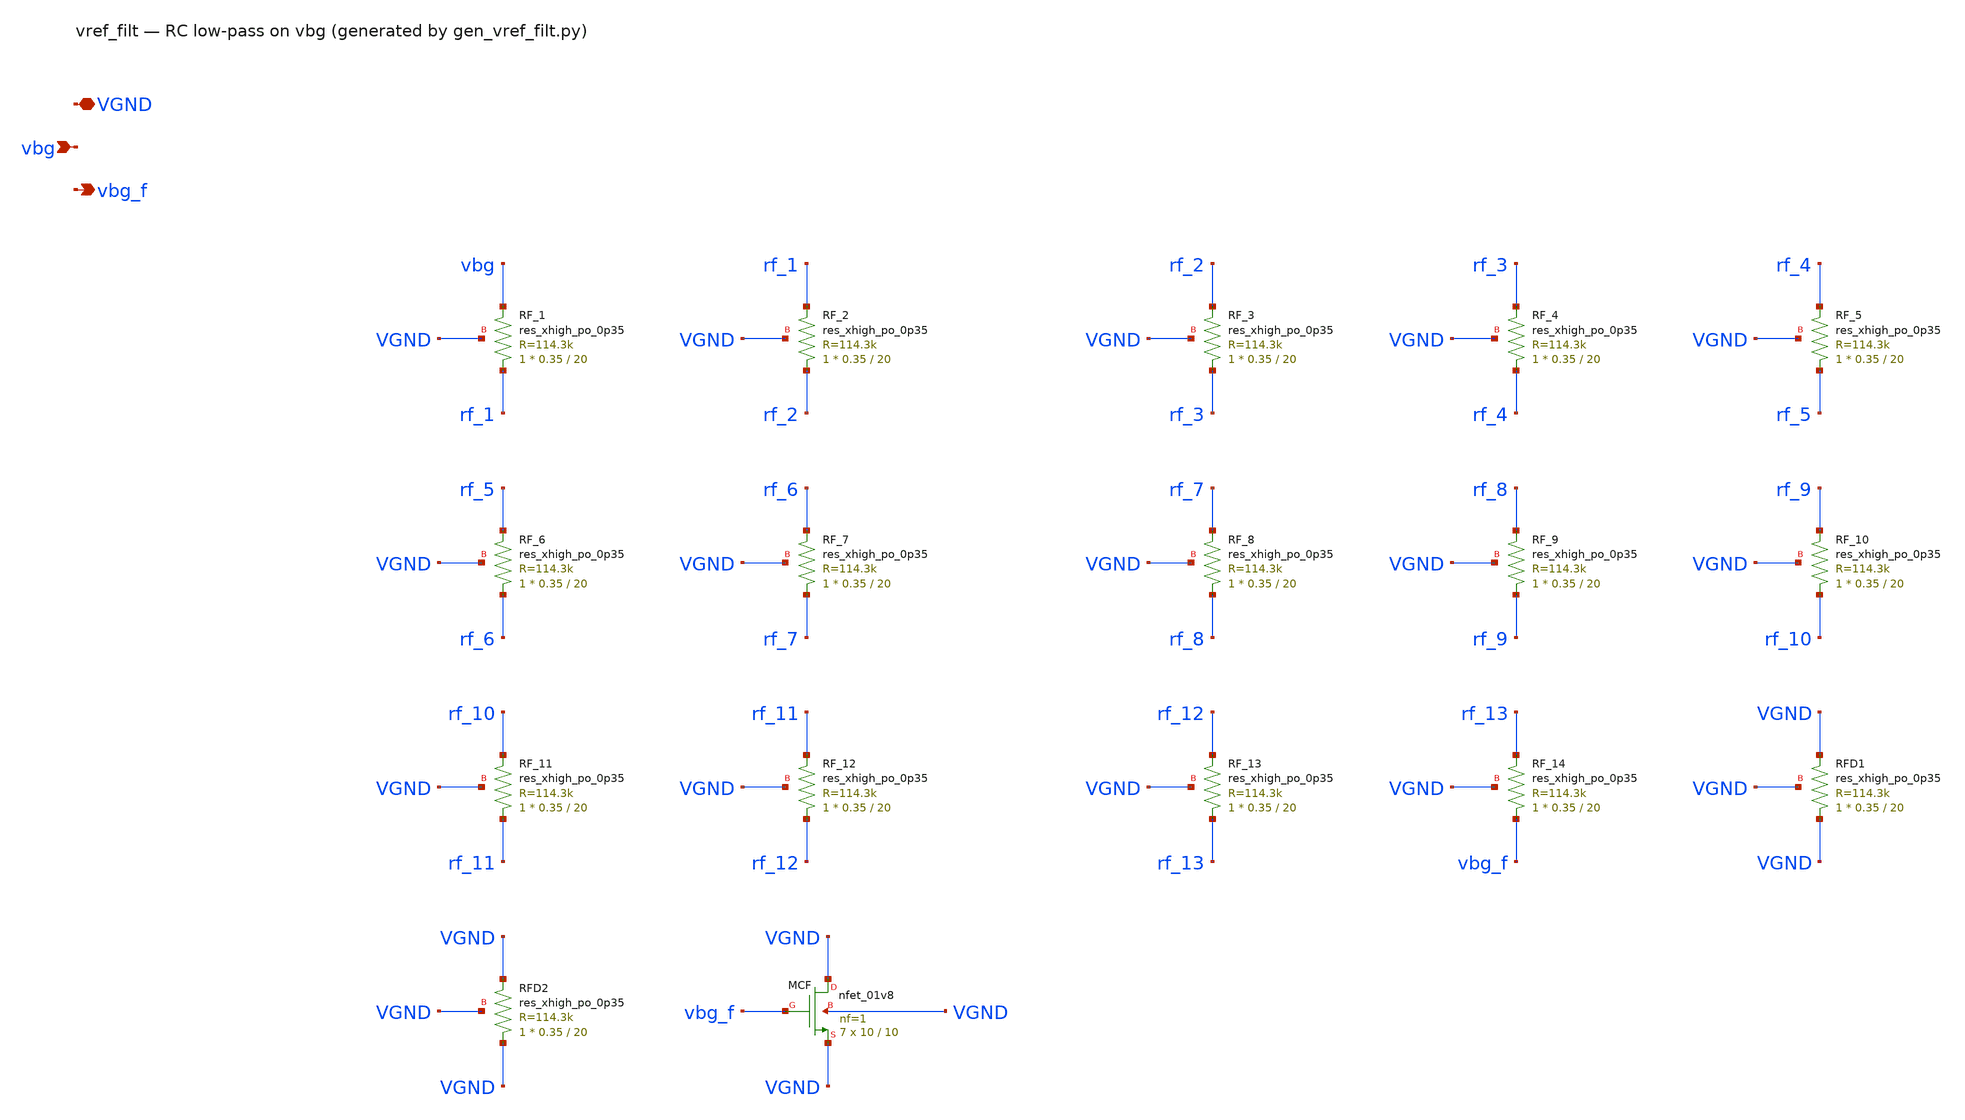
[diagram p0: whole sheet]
** sch_path: xschem/vref_filt.sch
**.subckt vref_filt VGND vbg vbg_f
*.iopin VGND
*.ipin vbg
*.opin vbg_f
XRF_1 rf_1 vbg VGND sky130_fd_pr__res_xhigh_po_0p35 L=20 mult=1 m=1
XRF_2 rf_2 rf_1 VGND sky130_fd_pr__res_xhigh_po_0p35 L=20 mult=1 m=1
XRF_3 rf_3 rf_2 VGND sky130_fd_pr__res_xhigh_po_0p35 L=20 mult=1 m=1
XRF_4 rf_4 rf_3 VGND sky130_fd_pr__res_xhigh_po_0p35 L=20 mult=1 m=1
XRF_5 rf_5 rf_4 VGND sky130_fd_pr__res_xhigh_po_0p35 L=20 mult=1 m=1
XRF_6 rf_6 rf_5 VGND sky130_fd_pr__res_xhigh_po_0p35 L=20 mult=1 m=1
XRF_7 rf_7 rf_6 VGND sky130_fd_pr__res_xhigh_po_0p35 L=20 mult=1 m=1
XRF_8 rf_8 rf_7 VGND sky130_fd_pr__res_xhigh_po_0p35 L=20 mult=1 m=1
XRF_9 rf_9 rf_8 VGND sky130_fd_pr__res_xhigh_po_0p35 L=20 mult=1 m=1
XRF_10 rf_10 rf_9 VGND sky130_fd_pr__res_xhigh_po_0p35 L=20 mult=1 m=1
XRF_11 rf_11 rf_10 VGND sky130_fd_pr__res_xhigh_po_0p35 L=20 mult=1 m=1
XRF_12 rf_12 rf_11 VGND sky130_fd_pr__res_xhigh_po_0p35 L=20 mult=1 m=1
XRF_13 rf_13 rf_12 VGND sky130_fd_pr__res_xhigh_po_0p35 L=20 mult=1 m=1
XRF_14 vbg_f rf_13 VGND sky130_fd_pr__res_xhigh_po_0p35 L=20 mult=1 m=1
XRFD1 VGND VGND VGND sky130_fd_pr__res_xhigh_po_0p35 L=20 mult=1 m=1
XRFD2 VGND VGND VGND sky130_fd_pr__res_xhigh_po_0p35 L=20 mult=1 m=1
XMCF VGND vbg_f VGND VGND sky130_fd_pr__nfet_01v8 L=10 W=10 nf=1 ad='int((1 + 1)/2) * 10 / 1 * 0.29'
+ as='int((1 + 2)/2) * 10 / 1 * 0.29' pd='2*int((1 + 1)/2) * (10 / 1 + 0.29)' ps='2*int((1 + 2)/2) * (10 / 1 + 0.29)'
+ nrd='0.29 / 10 ' nrs='0.29 / 10 ' sa=0 sb=0 sd=0 mult=7 m=7
**.ends
.end
